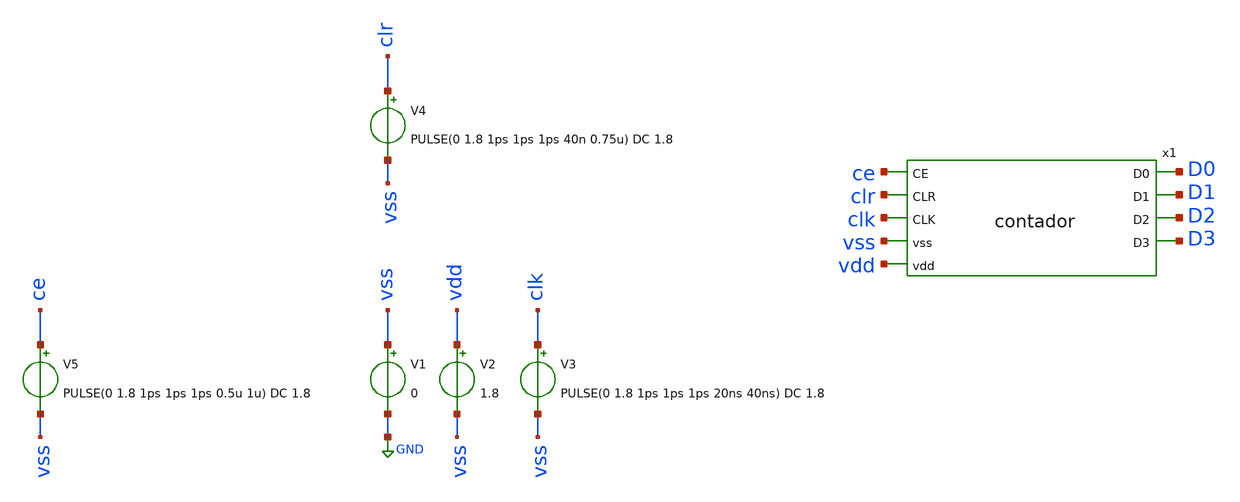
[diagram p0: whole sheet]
** sch_path: track_vlsi/toplevel_vlsi/sch/tb_contador.sch
**.subckt tb_contador
V1 vss GND 0
V2 vdd vss 1.8
V3 clk vss PULSE(0 1.8 1ps 1ps 1ps 20ns 40ns) DC 1.8
x1 D0 ce clr clk vss vdd D1 D2 D3 contador
V5 ce vss PULSE(0 1.8 1ps 1ps 1ps 0.5u 1u) DC 1.8
V4 clr vss PULSE(0 1.8 1ps 1ps 1ps 40n 0.75u) DC 1.8
**** begin user architecture code



* Parametros del circuito

.options TEMP = 27.0

* Include
.lib /home/eamta/skywater/skywater-pdk/libraries/sky130_fd_pr_ngspice/latest/models/corners/sky130.lib TT

* Signals to SAVE
*.save all
*+ @M.x1.XM1.msky130_fd_pr__nfet_01v8[id] @M.x1.XM1.msky130_fd_pr__nfet_01v8[gm]
*+ @M.x1.XM2.msky130_fd_pr__pfet_01v8[id] @M.x1.XM2.msky130_fd_pr__pfet_01v8[gm]

* Simulation
.control
  tran 1n 1us
  setplot tran1
  plot v(clk)
  plot v(D0)
  plot v(D1)
  plot v(D2)
  plot v(D3)
  plot v(ce)
  plot v(clr)
  write tb_contador_tran.raw

*reset
  *dc V1 0 1.8 0.01
  *setplot dc1
  *plot v(clk)
  *write tb_contador_dc.raw

  *reset
  *op
  *write tb_contador.raw
  *print all


.endc

.end


**** end user architecture code
**.ends
.GLOBAL GND
.end
